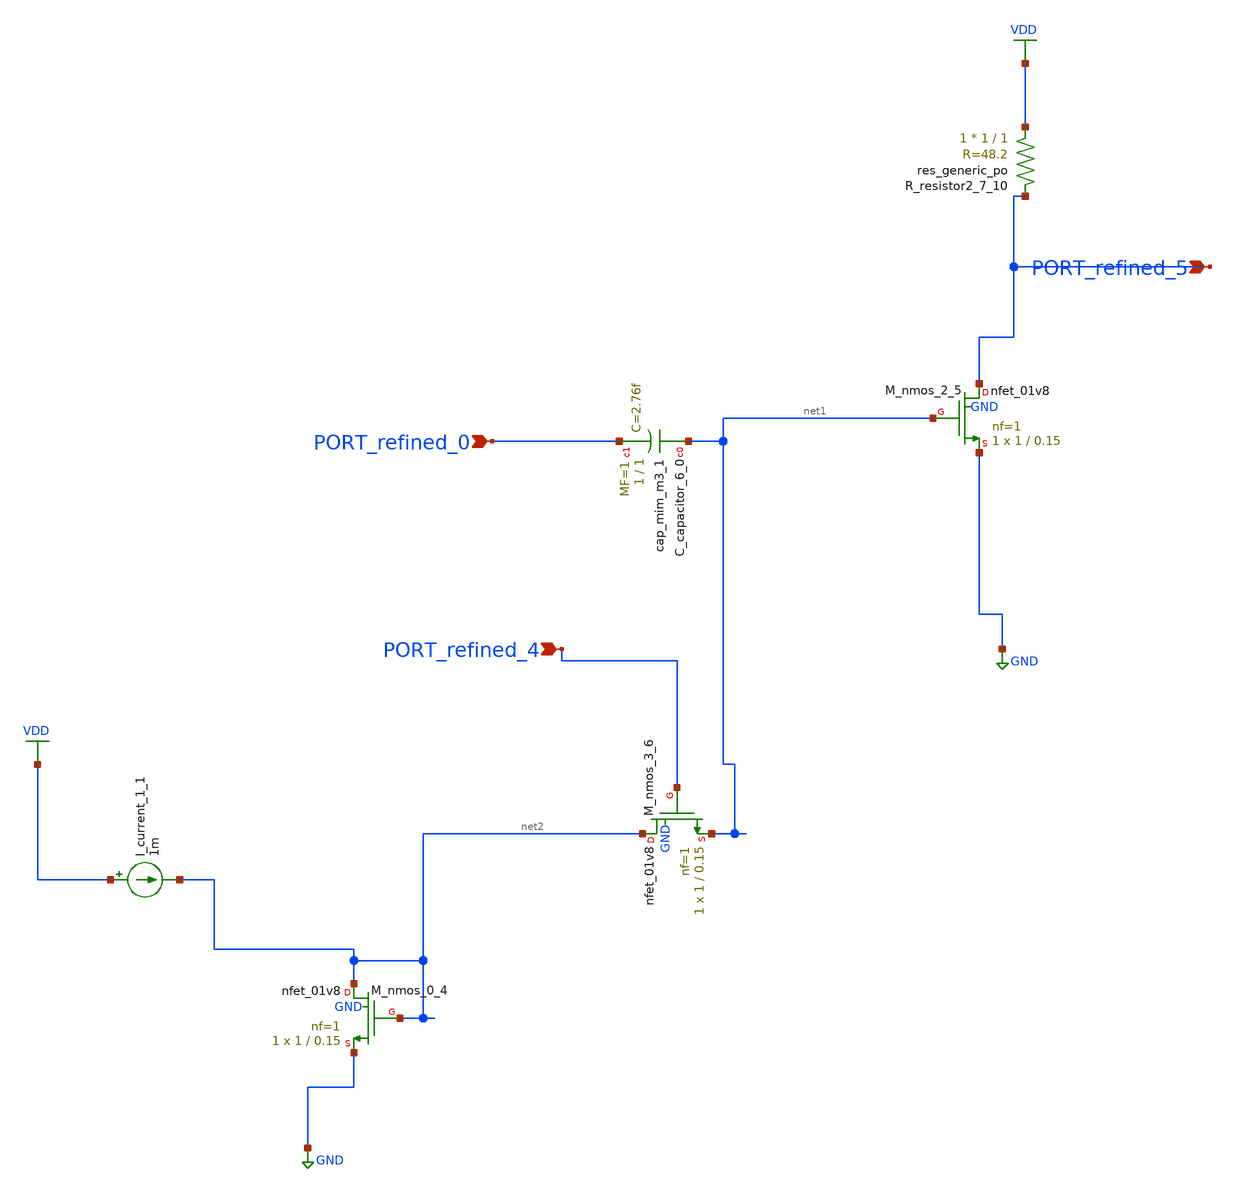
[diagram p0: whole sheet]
** sch_path: schematics/AMSNet/301.sch
**.subckt 301 PORT_refined_4 PORT_refined_5 PORT_refined_0
*.ipin PORT_refined_4
*.ipin PORT_refined_5
*.ipin PORT_refined_0
XC_capacitor_6_0 net1 PORT_refined_0 sky130_fd_pr__cap_mim_m3_1 W=1 L=1 MF=1 m=1
I_current_1_1 VDD net2 1m
XM_nmos_0_4 net2 net2 GND GND sky130_fd_pr__nfet_01v8 L=0.15 W=1 nf=1 ad='int((1 + 1)/2) * 1 / 1 * 0.29'
+ as='int((1 + 2)/2) * 1 / 1 * 0.29' pd='2*int((1 + 1)/2) * (1 / 1 + 0.29)' ps='2*int((1 + 2)/2) * (1 / 1 + 0.29)'
+ nrd='0.29 / 1 ' nrs='0.29 / 1 ' sa=0 sb=0 sd=0 mult=1 m=1
XM_nmos_2_5 PORT_refined_5 net1 GND GND sky130_fd_pr__nfet_01v8 L=0.15 W=1 nf=1 ad='int((1 + 1)/2) * 1 / 1 * 0.29'
+ as='int((1 + 2)/2) * 1 / 1 * 0.29' pd='2*int((1 + 1)/2) * (1 / 1 + 0.29)' ps='2*int((1 + 2)/2) * (1 / 1 + 0.29)'
+ nrd='0.29 / 1 ' nrs='0.29 / 1 ' sa=0 sb=0 sd=0 mult=1 m=1
XM_nmos_3_6 net2 PORT_refined_4 net1 GND sky130_fd_pr__nfet_01v8 L=0.15 W=1 nf=1 ad='int((1 + 1)/2) * 1 / 1 * 0.29'
+ as='int((1 + 2)/2) * 1 / 1 * 0.29' pd='2*int((1 + 1)/2) * (1 / 1 + 0.29)' ps='2*int((1 + 2)/2) * (1 / 1 + 0.29)'
+ nrd='0.29 / 1 ' nrs='0.29 / 1 ' sa=0 sb=0 sd=0 mult=1 m=1
XR_resistor2_7_10 VDD PORT_refined_5 sky130_fd_pr__res_generic_po W=1 L=1 m=1
**.ends
.GLOBAL GND
.GLOBAL VDD
.end
